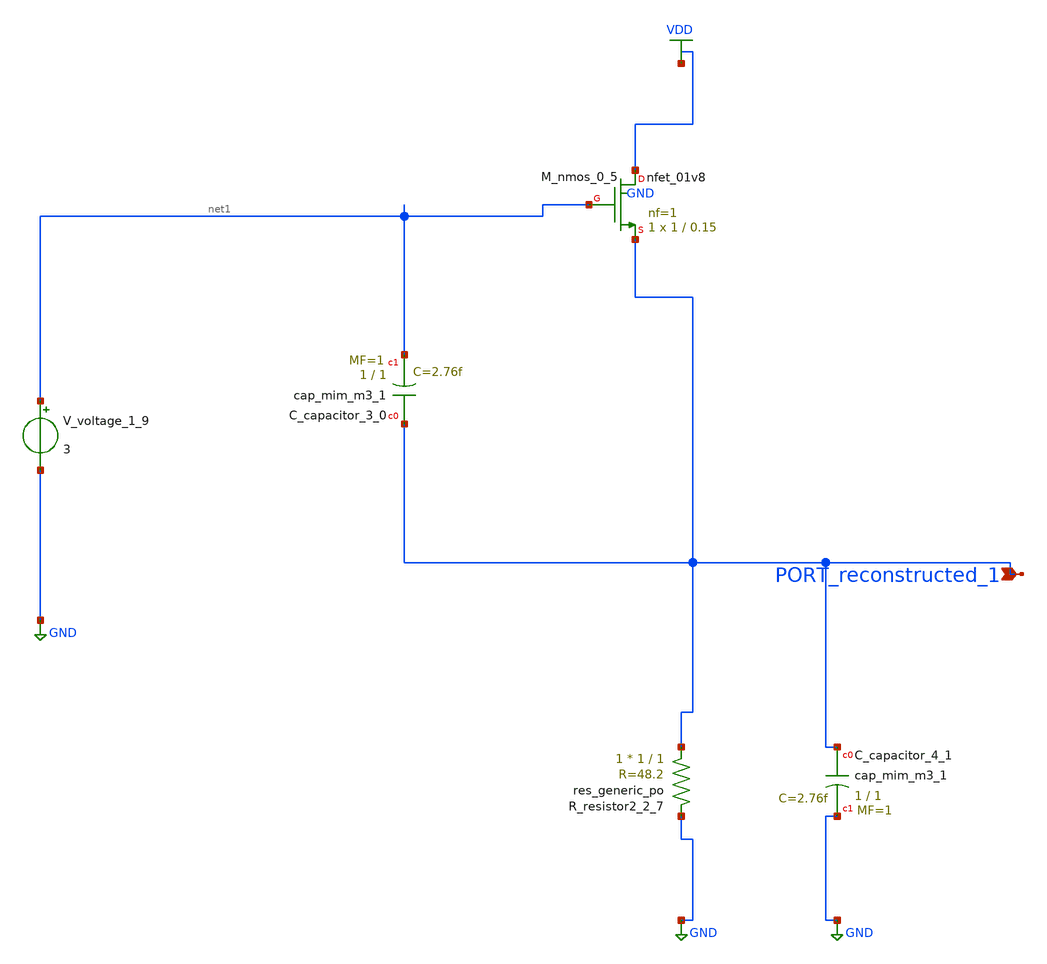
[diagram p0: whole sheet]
** sch_path: schematics/AMSNet/370.sch
**.subckt 370 PORT_reconstructed_1
*.ipin PORT_reconstructed_1
XC_capacitor_3_0 PORT_reconstructed_1 net1 sky130_fd_pr__cap_mim_m3_1 W=1 L=1 MF=1 m=1
XC_capacitor_4_1 PORT_reconstructed_1 GND sky130_fd_pr__cap_mim_m3_1 W=1 L=1 MF=1 m=1
XM_nmos_0_5 VDD net1 PORT_reconstructed_1 GND sky130_fd_pr__nfet_01v8 L=0.15 W=1 nf=1 ad='int((1 + 1)/2) * 1 / 1 * 0.29'
+ as='int((1 + 2)/2) * 1 / 1 * 0.29' pd='2*int((1 + 1)/2) * (1 / 1 + 0.29)' ps='2*int((1 + 2)/2) * (1 / 1 + 0.29)'
+ nrd='0.29 / 1 ' nrs='0.29 / 1 ' sa=0 sb=0 sd=0 mult=1 m=1
XR_resistor2_2_7 PORT_reconstructed_1 GND sky130_fd_pr__res_generic_po W=1 L=1 m=1
V_voltage_1_9 net1 GND 3
**.ends
.GLOBAL GND
.GLOBAL VDD
.end
